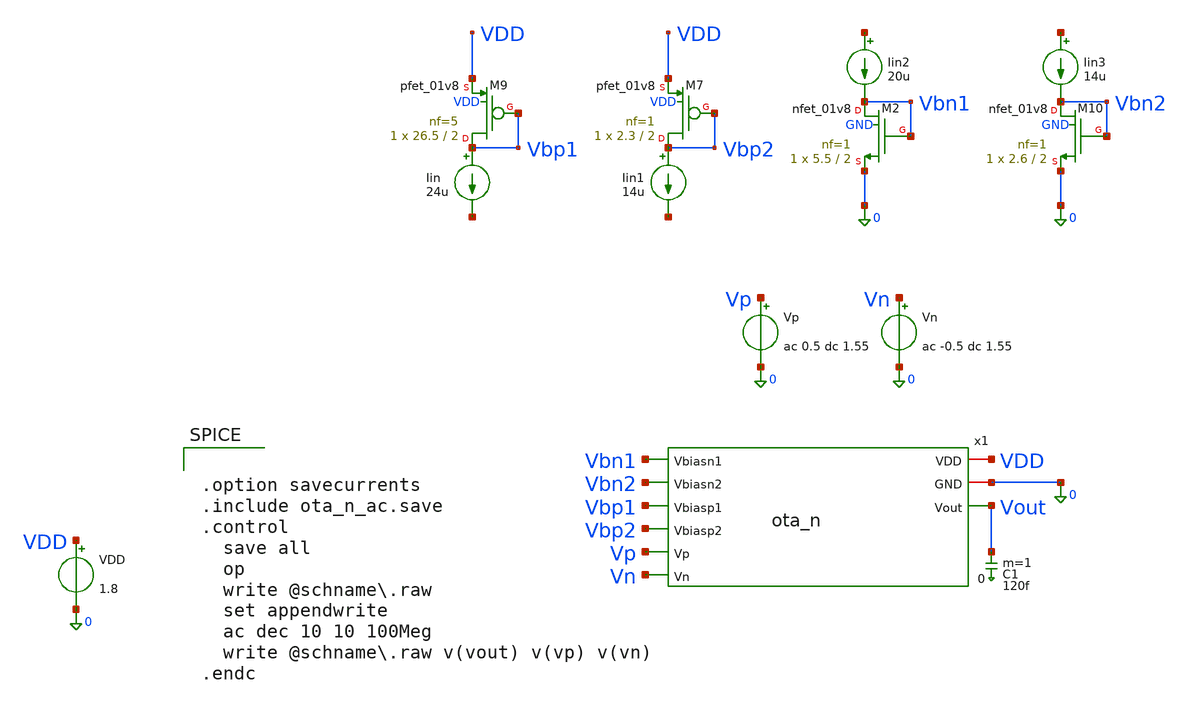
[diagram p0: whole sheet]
** sch_path: sch/cascode/ota_n_ac.sch
**.subckt ota_n_ac
Iin Vbp1 net1 24u
VDD VDD 0 1.8
.save i(vdd)
Vp Vp 0 ac 0.5 dc 1.55
.save i(vp)
Vn Vn 0 ac -0.5 dc 1.55
.save i(vn)
C1 Vout 0 120f m=1
x1 VDD 0 Vbn1 Vbn2 Vbp1 Vbp2 Vp Vn Vout ota_n
Iin1 Vbp2 net2 14u
Iin2 net3 Vbn1 20u
Iin3 net4 Vbn2 14u
XM9 Vbp1 Vbp1 VDD VDD sky130_fd_pr__pfet_01v8 L=2 W=26.5 nf=5 ad='int((5 + 1)/2) * 26.5 / 5 * 0.29' as='int((5 + 2)/2) * 26.5 / 5 * 0.29'
+ pd='2*int((5 + 1)/2) * (26.5 / 5 + 0.29)' ps='2*int((5 + 2)/2) * (26.5 / 5 + 0.29)' nrd='0.29 / 26.5 '
+ nrs='0.29 / 26.5 ' sa=0 sb=0 sd=0 mult=1 m=1
XM7 Vbp2 Vbp2 VDD VDD sky130_fd_pr__pfet_01v8 L=2 W=2.3 nf=1 ad='int((1 + 1)/2) * 2.3 / 1 * 0.29' as='int((1 + 2)/2) * 2.3 / 1 * 0.29'
+ pd='2*int((1 + 1)/2) * (2.3 / 1 + 0.29)' ps='2*int((1 + 2)/2) * (2.3 / 1 + 0.29)' nrd='0.29 / 2.3 ' nrs='0.29 / 2.3 '
+ sa=0 sb=0 sd=0 mult=1 m=1
XM10 Vbn2 Vbn2 0 GND sky130_fd_pr__nfet_01v8 L=2 W=2.6 nf=1 ad='int((1 + 1)/2) * 2.6 / 1 * 0.29' as='int((1 + 2)/2) * 2.6 / 1 * 0.29'
+ pd='2*int((1 + 1)/2) * (2.6 / 1 + 0.29)' ps='2*int((1 + 2)/2) * (2.6 / 1 + 0.29)' nrd='0.29 / 2.6 ' nrs='0.29 / 2.6 '
+ sa=0 sb=0 sd=0 mult=1 m=1
XM2 Vbn1 Vbn1 0 GND sky130_fd_pr__nfet_01v8 L=2 W=5.5 nf=1 ad='int((1 + 1)/2) * 5.5 / 1 * 0.29' as='int((1 + 2)/2) * 5.5 / 1 * 0.29'
+ pd='2*int((1 + 1)/2) * (5.5 / 1 + 0.29)' ps='2*int((1 + 2)/2) * (5.5 / 1 + 0.29)' nrd='0.29 / 5.5 ' nrs='0.29 / 5.5 '
+ sa=0 sb=0 sd=0 mult=1 m=1
**** begin user architecture code

** opencircuitdesign pdks install
.lib $::SKYWATER_MODELS/sky130.lib.spice tt
.include $::SKYWATER_STDCELLS/sky130_fd_sc_hd.spice



.option savecurrents
.include ota_n_ac.save
.control
  save all
  op
  write @schname\.raw
  set appendwrite
  ac dec 10 10 100Meg
  write @schname\.raw v(vout) v(vp) v(vn)
.endc


**** end user architecture code
**.ends

* expanding   symbol:  /foss/designs/sar_adc/sch/cascode/ota_n.sym # of pins=9
** sym_path: sch/cascode/ota_n.sym
** sch_path: sch/cascode/ota_n.sch
.subckt ota_n VDD GND Vbiasn1 Vbiasn2 Vbiasp1 Vbiasp2 Vp Vn Vout
*.ipin Vbiasn2
*.opin Vout
*.iopin VDD
*.iopin GND
*.ipin Vp
*.ipin Vn
*.ipin Vbiasp1
*.ipin Vbiasp2
*.ipin Vbiasn1
XM3 net1 Vp Vx GND sky130_fd_pr__nfet_01v8 L=2 W=7.5 nf=1 ad='int((1 + 1)/2) * 7.5 / 1 * 0.29' as='int((1 + 2)/2) * 7.5 / 1 * 0.29'
+ pd='2*int((1 + 1)/2) * (7.5 / 1 + 0.29)' ps='2*int((1 + 2)/2) * (7.5 / 1 + 0.29)' nrd='0.29 / 7.5 ' nrs='0.29 / 7.5 '
+ sa=0 sb=0 sd=0 mult=1 m=1
XM2 Vfold Vn Vx GND sky130_fd_pr__nfet_01v8 L=2 W=7.5 nf=1 ad='int((1 + 1)/2) * 7.5 / 1 * 0.29' as='int((1 + 2)/2) * 7.5 / 1 * 0.29'
+ pd='2*int((1 + 1)/2) * (7.5 / 1 + 0.29)' ps='2*int((1 + 2)/2) * (7.5 / 1 + 0.29)' nrd='0.29 / 7.5 ' nrs='0.29 / 7.5 '
+ sa=0 sb=0 sd=0 mult=1 m=1
XM4 net3 net2 GND GND sky130_fd_pr__nfet_01v8 L=2 W=14 nf=2 ad='int((2 + 1)/2) * 14 / 2 * 0.29' as='int((2 + 2)/2) * 14 / 2 * 0.29'
+ pd='2*int((2 + 1)/2) * (14 / 2 + 0.29)' ps='2*int((2 + 2)/2) * (14 / 2 + 0.29)' nrd='0.29 / 14 ' nrs='0.29 / 14 '
+ sa=0 sb=0 sd=0 mult=1 m=1
XM5 net4 net2 GND GND sky130_fd_pr__nfet_01v8 L=2 W=14 nf=2 ad='int((2 + 1)/2) * 14 / 2 * 0.29' as='int((2 + 2)/2) * 14 / 2 * 0.29'
+ pd='2*int((2 + 1)/2) * (14 / 2 + 0.29)' ps='2*int((2 + 2)/2) * (14 / 2 + 0.29)' nrd='0.29 / 14 ' nrs='0.29 / 14 '
+ sa=0 sb=0 sd=0 mult=1 m=1
XM8 net1 Vbiasp1 VDD VDD sky130_fd_pr__pfet_01v8 L=2 W=26.5 nf=5 ad='int((5 + 1)/2) * 26.5 / 5 * 0.29'
+ as='int((5 + 2)/2) * 26.5 / 5 * 0.29' pd='2*int((5 + 1)/2) * (26.5 / 5 + 0.29)' ps='2*int((5 + 2)/2) * (26.5 / 5 + 0.29)'
+ nrd='0.29 / 26.5 ' nrs='0.29 / 26.5 ' sa=0 sb=0 sd=0 mult=1 m=1
XM9 Vfold Vbiasp1 VDD VDD sky130_fd_pr__pfet_01v8 L=2 W=26.5 nf=5 ad='int((5 + 1)/2) * 26.5 / 5 * 0.29'
+ as='int((5 + 2)/2) * 26.5 / 5 * 0.29' pd='2*int((5 + 1)/2) * (26.5 / 5 + 0.29)' ps='2*int((5 + 2)/2) * (26.5 / 5 + 0.29)'
+ nrd='0.29 / 26.5 ' nrs='0.29 / 26.5 ' sa=0 sb=0 sd=0 mult=1 m=1
XM1 Vx Vbiasn1 GND GND sky130_fd_pr__nfet_01v8 L=2 W=5.5 nf=1 ad='int((1 + 1)/2) * 5.5 / 1 * 0.29' as='int((1 + 2)/2) * 5.5 / 1 * 0.29'
+ pd='2*int((1 + 1)/2) * (5.5 / 1 + 0.29)' ps='2*int((1 + 2)/2) * (5.5 / 1 + 0.29)' nrd='0.29 / 5.5 ' nrs='0.29 / 5.5 '
+ sa=0 sb=0 sd=0 mult=1 m=1
XM6 net2 Vbiasp2 net1 VDD sky130_fd_pr__pfet_01v8 L=2 W=13 nf=2 ad='int((2 + 1)/2) * 13 / 2 * 0.29' as='int((2 + 2)/2) * 13 / 2 * 0.29'
+ pd='2*int((2 + 1)/2) * (13 / 2 + 0.29)' ps='2*int((2 + 2)/2) * (13 / 2 + 0.29)' nrd='0.29 / 13 ' nrs='0.29 / 13 '
+ sa=0 sb=0 sd=0 mult=1 m=1
XM7 Vout Vbiasp2 Vfold VDD sky130_fd_pr__pfet_01v8 L=2 W=13 nf=2 ad='int((2 + 1)/2) * 13 / 2 * 0.29'
+ as='int((2 + 2)/2) * 13 / 2 * 0.29' pd='2*int((2 + 1)/2) * (13 / 2 + 0.29)' ps='2*int((2 + 2)/2) * (13 / 2 + 0.29)'
+ nrd='0.29 / 13 ' nrs='0.29 / 13 ' sa=0 sb=0 sd=0 mult=1 m=1
XM10 Vout Vbiasn2 net4 GND sky130_fd_pr__nfet_01v8 L=2 W=26.5 nf=5 ad='int((5 + 1)/2) * 26.5 / 5 * 0.29'
+ as='int((5 + 2)/2) * 26.5 / 5 * 0.29' pd='2*int((5 + 1)/2) * (26.5 / 5 + 0.29)' ps='2*int((5 + 2)/2) * (26.5 / 5 + 0.29)'
+ nrd='0.29 / 26.5 ' nrs='0.29 / 26.5 ' sa=0 sb=0 sd=0 mult=1 m=1
XM11 net2 Vbiasn2 net3 GND sky130_fd_pr__nfet_01v8 L=2 W=26.5 nf=5 ad='int((5 + 1)/2) * 26.5 / 5 * 0.29'
+ as='int((5 + 2)/2) * 26.5 / 5 * 0.29' pd='2*int((5 + 1)/2) * (26.5 / 5 + 0.29)' ps='2*int((5 + 2)/2) * (26.5 / 5 + 0.29)'
+ nrd='0.29 / 26.5 ' nrs='0.29 / 26.5 ' sa=0 sb=0 sd=0 mult=1 m=1
.ends

.end
